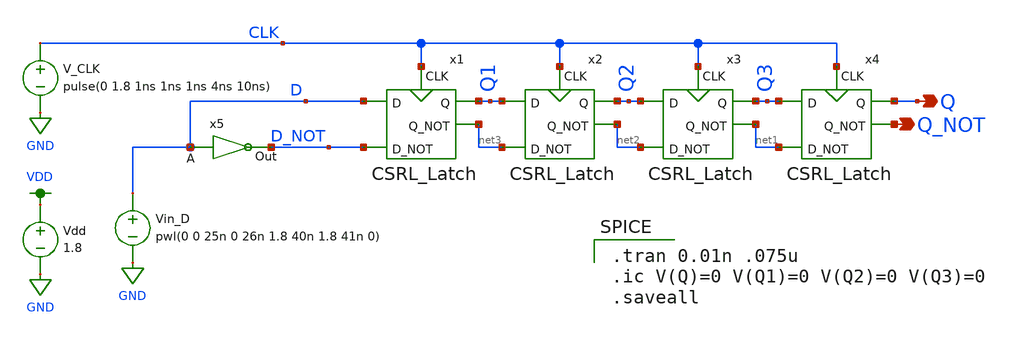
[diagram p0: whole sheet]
** sch_path: miniproject2/MP2_LAB_2.sch
**.subckt MP2_LAB_2 Q Q_NOT
*.opin Q
*.opin Q_NOT
x1 D Q1 D_NOT net3 CLK CSRL_Latch
x2 Q1 Q2 net3 net2 CLK CSRL_Latch
x3 Q2 Q3 net2 net1 CLK CSRL_Latch
x4 Q3 Q net1 Q_NOT CLK CSRL_Latch
Vin_D D GND pwl(0 0 25n 0 26n 1.8 40n 1.8 41n 0)
V_CLK CLK GND pulse(0 1.8 1ns 1ns 1ns 4ns 10ns)
Vdd VDD GND 1.8
x5 D_NOT D MP1_inverter
**** begin user architecture code

.tran 0.01n .075u
.ic V(Q)=0 V(Q1)=0 V(Q2)=0 V(Q3)=0
.saveall


.option wnflag=1
.lib ~/skywater/skywater-pdk/libraries/sky130_fd_pr_ngspice/latest/models/sky130.lib.spice tt

**** end user architecture code
**.ends

* expanding   symbol:  /home/lxbtlr/MAD/miniproject2/CSRL_Latch.sym # of pins=5
** sym_path: miniproject2/CSRL_Latch.sym
** sch_path: miniproject2/CSRL_Latch.sch
.subckt CSRL_Latch D Q D_NOT Q_NOT CLK
*.ipin D
*.ipin D_NOT
*.opin Q
*.opin Q_NOT
*.ipin CLK
XQ8 net1 net2 VDD VDD sky130_fd_pr__pfet_01v8 L=0.15 W=1 nf=1 ad='int((nf+1)/2) * W/nf * 0.29' as='int((nf+2)/2) * W/nf * 0.29'
+ pd='2*int((nf+1)/2) * (W/nf + 0.29)' ps='2*int((nf+2)/2) * (W/nf + 0.29)' nrd='0.29 / W' nrs='0.29 / W'
+ sa=0 sb=0 sd=0 mult=1 m=1
XQ9 VDD net1 net2 VDD sky130_fd_pr__pfet_01v8 L=0.15 W=1 nf=1 ad='int((nf+1)/2) * W/nf * 0.29' as='int((nf+2)/2) * W/nf * 0.29'
+ pd='2*int((nf+1)/2) * (W/nf + 0.29)' ps='2*int((nf+2)/2) * (W/nf + 0.29)' nrd='0.29 / W' nrs='0.29 / W'
+ sa=0 sb=0 sd=0 mult=1 m=1
XQ1 net2 CLK D VDD sky130_fd_pr__pfet_01v8 L=0.15 W=1 nf=1 ad='int((nf+1)/2) * W/nf * 0.29' as='int((nf+2)/2) * W/nf * 0.29'
+ pd='2*int((nf+1)/2) * (W/nf + 0.29)' ps='2*int((nf+2)/2) * (W/nf + 0.29)' nrd='0.29 / W' nrs='0.29 / W'
+ sa=0 sb=0 sd=0 mult=1 m=1
XQ2 net1 CLK D_NOT VDD sky130_fd_pr__pfet_01v8 L=0.15 W=1 nf=1 ad='int((nf+1)/2) * W/nf * 0.29' as='int((nf+2)/2) * W/nf * 0.29'
+ pd='2*int((nf+1)/2) * (W/nf + 0.29)' ps='2*int((nf+2)/2) * (W/nf + 0.29)' nrd='0.29 / W' nrs='0.29 / W'
+ sa=0 sb=0 sd=0 mult=1 m=1
XQ5 net4 CLK GND GND sky130_fd_pr__nfet_01v8 L=0.15 W=4 nf=1 ad='int((nf+1)/2) * W/nf * 0.29' as='int((nf+2)/2) * W/nf * 0.29'
+ pd='2*int((nf+1)/2) * (W/nf + 0.29)' ps='2*int((nf+2)/2) * (W/nf + 0.29)' nrd='0.29 / W' nrs='0.29 / W'
+ sa=0 sb=0 sd=0 mult=1 m=1
XQ4 Q_NOT CLK net1 GND sky130_fd_pr__nfet_01v8 L=0.15 W=1 nf=1 ad='int((nf+1)/2) * W/nf * 0.29' as='int((nf+2)/2) * W/nf * 0.29'
+ pd='2*int((nf+1)/2) * (W/nf + 0.29)' ps='2*int((nf+2)/2) * (W/nf + 0.29)' nrd='0.29 / W' nrs='0.29 / W'
+ sa=0 sb=0 sd=0 mult=1 m=1
XQ3 Q CLK net2 GND sky130_fd_pr__nfet_01v8 L=0.15 W=1 nf=1 ad='int((nf+1)/2) * W/nf * 0.29' as='int((nf+2)/2) * W/nf * 0.29'
+ pd='2*int((nf+1)/2) * (W/nf + 0.29)' ps='2*int((nf+2)/2) * (W/nf + 0.29)' nrd='0.29 / W' nrs='0.29 / W'
+ sa=0 sb=0 sd=0 mult=1 m=1
XQ6 net1 net2 net4 GND sky130_fd_pr__nfet_01v8 L=0.15 W=1 nf=1 ad='int((nf+1)/2) * W/nf * 0.29' as='int((nf+2)/2) * W/nf * 0.29'
+ pd='2*int((nf+1)/2) * (W/nf + 0.29)' ps='2*int((nf+2)/2) * (W/nf + 0.29)' nrd='0.29 / W' nrs='0.29 / W'
+ sa=0 sb=0 sd=0 mult=1 m=1
XQ7 net4 net1 net2 GND sky130_fd_pr__nfet_01v8 L=0.15 W=1 nf=1 ad='int((nf+1)/2) * W/nf * 0.29' as='int((nf+2)/2) * W/nf * 0.29'
+ pd='2*int((nf+1)/2) * (W/nf + 0.29)' ps='2*int((nf+2)/2) * (W/nf + 0.29)' nrd='0.29 / W' nrs='0.29 / W'
+ sa=0 sb=0 sd=0 mult=1 m=1
XQ13 Q_NOT Q GND GND sky130_fd_pr__nfet_01v8 L=0.15 W=1 nf=1 ad='int((nf+1)/2) * W/nf * 0.29' as='int((nf+2)/2) * W/nf * 0.29'
+ pd='2*int((nf+1)/2) * (W/nf + 0.29)' ps='2*int((nf+2)/2) * (W/nf + 0.29)' nrd='0.29 / W' nrs='0.29 / W'
+ sa=0 sb=0 sd=0 mult=1 m=1
XQ14 GND Q_NOT Q GND sky130_fd_pr__nfet_01v8 L=0.15 W=1 nf=1 ad='int((nf+1)/2) * W/nf * 0.29' as='int((nf+2)/2) * W/nf * 0.29'
+ pd='2*int((nf+1)/2) * (W/nf + 0.29)' ps='2*int((nf+2)/2) * (W/nf + 0.29)' nrd='0.29 / W' nrs='0.29 / W'
+ sa=0 sb=0 sd=0 mult=1 m=1
XQ11 Q_NOT Q net3 VDD sky130_fd_pr__pfet_01v8 L=0.15 W=1 nf=1 ad='int((nf+1)/2) * W/nf * 0.29' as='int((nf+2)/2) * W/nf * 0.29'
+ pd='2*int((nf+1)/2) * (W/nf + 0.29)' ps='2*int((nf+2)/2) * (W/nf + 0.29)' nrd='0.29 / W' nrs='0.29 / W'
+ sa=0 sb=0 sd=0 mult=1 m=1
XQ12 net3 Q_NOT Q VDD sky130_fd_pr__pfet_01v8 L=0.15 W=1 nf=1 ad='int((nf+1)/2) * W/nf * 0.29' as='int((nf+2)/2) * W/nf * 0.29'
+ pd='2*int((nf+1)/2) * (W/nf + 0.29)' ps='2*int((nf+2)/2) * (W/nf + 0.29)' nrd='0.29 / W' nrs='0.29 / W'
+ sa=0 sb=0 sd=0 mult=1 m=1
XQ10 net3 CLK VDD VDD sky130_fd_pr__pfet_01v8 L=0.15 W=4 nf=1 ad='int((nf+1)/2) * W/nf * 0.29' as='int((nf+2)/2) * W/nf * 0.29'
+ pd='2*int((nf+1)/2) * (W/nf + 0.29)' ps='2*int((nf+2)/2) * (W/nf + 0.29)' nrd='0.29 / W' nrs='0.29 / W'
+ sa=0 sb=0 sd=0 mult=1 m=1
.ends


* expanding   symbol:  /home/lxbtlr/MAD/miniproject1/MP1_inverter.sym # of pins=2
** sym_path: miniproject2/MP1_inverter.sym
** sch_path: miniproject2/MP1_inverter.sch
.subckt MP1_inverter Out A
*.ipin A
*.opin Out
XM1 Out A VDD VDD sky130_fd_pr__pfet_01v8 L=0.15 W=1 nf=1 ad='int((nf+1)/2) * W/nf * 0.29' as='int((nf+2)/2) * W/nf * 0.29'
+ pd='2*int((nf+1)/2) * (W/nf + 0.29)' ps='2*int((nf+2)/2) * (W/nf + 0.29)' nrd='0.29 / W' nrs='0.29 / W'
+ sa=0 sb=0 sd=0 mult=1 m=1
XM2 Out A GND GND sky130_fd_pr__nfet_01v8 L=0.15 W=1 nf=1 ad='int((nf+1)/2) * W/nf * 0.29' as='int((nf+2)/2) * W/nf * 0.29'
+ pd='2*int((nf+1)/2) * (W/nf + 0.29)' ps='2*int((nf+2)/2) * (W/nf + 0.29)' nrd='0.29 / W' nrs='0.29 / W'
+ sa=0 sb=0 sd=0 mult=1 m=1
.ends

.GLOBAL GND
.GLOBAL VDD
.end
